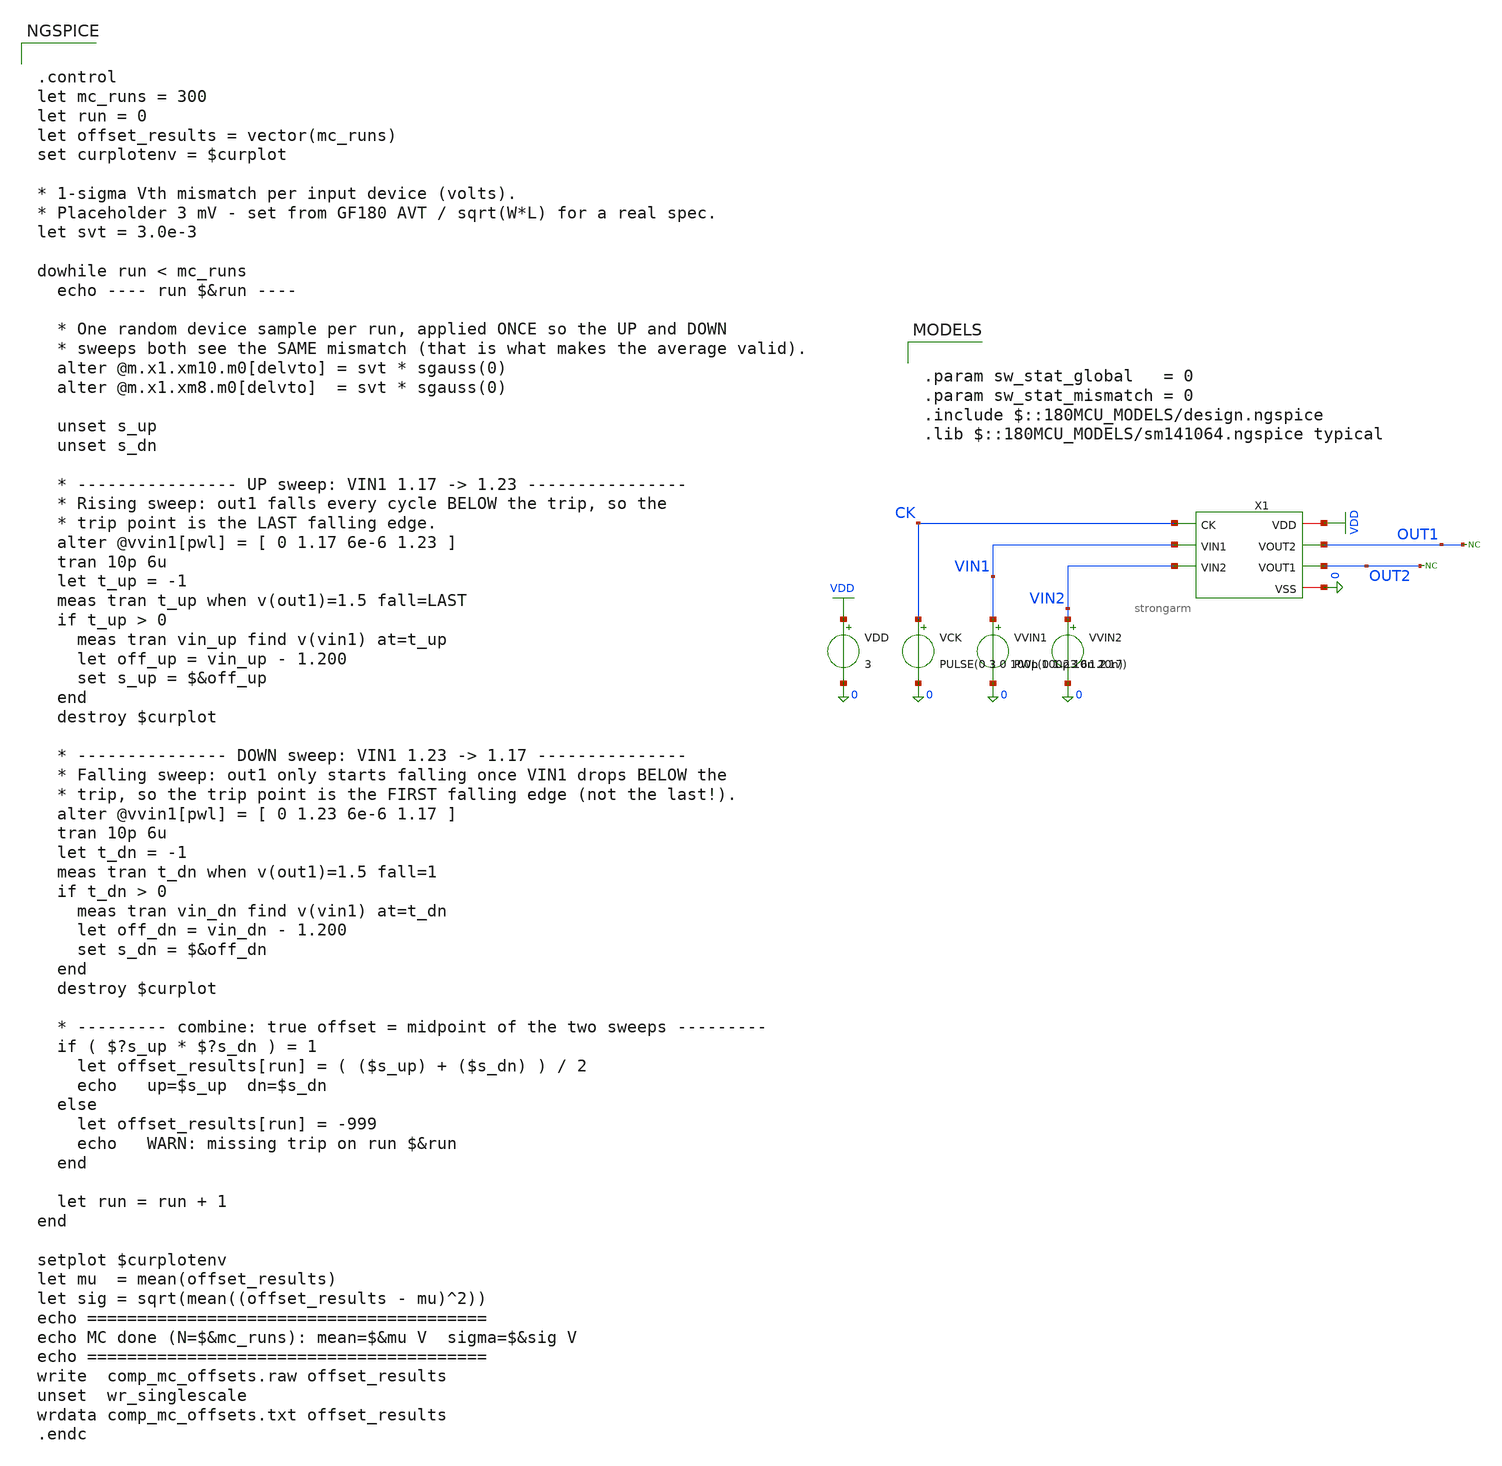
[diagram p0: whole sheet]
** sch_path: comparator/schematic/strongarm_mc_tb.sch
**.subckt strongarm_mc_tb
X1 VDD CK OUT1 OUT2 VIN1 VIN2 0 strongarm
VVIN2 VIN2 0 1.2
VVIN1 VIN1 0 PWL(0 1.23 6u 1.17)
VDD VDD 0 3
VCK CK 0 PULSE(0 3 0 100p 100p 10n 20n)
* noconn OUT2
* noconn OUT1
**** begin user architecture code

.param sw_stat_global   = 0
.param sw_stat_mismatch = 0
.include $::180MCU_MODELS/design.ngspice
.lib $::180MCU_MODELS/sm141064.ngspice typical



.control
let mc_runs = 300
let run = 0
let offset_results = vector(mc_runs)
set curplotenv = $curplot

* 1-sigma Vth mismatch per input device (volts).
* Placeholder 3 mV - set from GF180 AVT / sqrt(W*L) for a real spec.
let svt = 3.0e-3

dowhile run < mc_runs
  echo ---- run $&run ----

  * One random device sample per run, applied ONCE so the UP and DOWN
  * sweeps both see the SAME mismatch (that is what makes the average valid).
  alter @m.x1.xm10.m0[delvto] = svt * sgauss(0)
  alter @m.x1.xm8.m0[delvto]  = svt * sgauss(0)

  unset s_up
  unset s_dn

  * ---------------- UP sweep: VIN1 1.17 -> 1.23 ----------------
  * Rising sweep: out1 falls every cycle BELOW the trip, so the
  * trip point is the LAST falling edge.
  alter @vvin1[pwl] = [ 0 1.17 6e-6 1.23 ]
  tran 10p 6u
  let t_up = -1
  meas tran t_up when v(out1)=1.5 fall=LAST
  if t_up > 0
    meas tran vin_up find v(vin1) at=t_up
    let off_up = vin_up - 1.200
    set s_up = $&off_up
  end
  destroy $curplot

  * --------------- DOWN sweep: VIN1 1.23 -> 1.17 ---------------
  * Falling sweep: out1 only starts falling once VIN1 drops BELOW the
  * trip, so the trip point is the FIRST falling edge (not the last!).
  alter @vvin1[pwl] = [ 0 1.23 6e-6 1.17 ]
  tran 10p 6u
  let t_dn = -1
  meas tran t_dn when v(out1)=1.5 fall=1
  if t_dn > 0
    meas tran vin_dn find v(vin1) at=t_dn
    let off_dn = vin_dn - 1.200
    set s_dn = $&off_dn
  end
  destroy $curplot

  * --------- combine: true offset = midpoint of the two sweeps ---------
  if ( $?s_up * $?s_dn ) = 1
    let offset_results[run] = ( ($s_up) + ($s_dn) ) / 2
    echo   up=$s_up  dn=$s_dn
  else
    let offset_results[run] = -999
    echo   WARN: missing trip on run $&run
  end

  let run = run + 1
end

setplot $curplotenv
let mu  = mean(offset_results)
let sig = sqrt(mean((offset_results - mu)^2))
echo ========================================
echo MC done (N=$&mc_runs): mean=$&mu V  sigma=$&sig V
echo ========================================
write  comp_mc_offsets.raw offset_results
unset  wr_singlescale
wrdata comp_mc_offsets.txt offset_results
.endc


**** end user architecture code
**.ends

* expanding   symbol:  comparator/schematic/strongarm.sym # of pins=7
** sym_path: comparator/schematic/strongarm.sym
** sch_path: comparator/schematic/strongarm.sch
.subckt strongarm VDD CK VOUT2 VOUT1 VIN1 VIN2 VSS
*.opin VOUT1
*.opin VOUT2
*.ipin VIN1
*.ipin VIN2
*.ipin CK
*.iopin VDD
*.iopin VSS
XM1 VOUT2 VOUT1 net1 net1 nfet_03v3 L=0.28u W=0.22u nf=1 ad='int((nf+1)/2) * W/nf * 0.18u' as='int((nf+2)/2) * W/nf * 0.18u'
+ pd='2*int((nf+1)/2) * (W/nf + 0.18u)' ps='2*int((nf+2)/2) * (W/nf + 0.18u)' nrd='0.18u / W' nrs='0.18u / W'
+ sa=0 sb=0 sd=0 m=1
XM2 VOUT1 VOUT2 VDD VDD pfet_03v3 L=0.28u W=0.22u nf=1 ad='int((nf+1)/2) * W/nf * 0.18u' as='int((nf+2)/2) * W/nf * 0.18u'
+ pd='2*int((nf+1)/2) * (W/nf + 0.18u)' ps='2*int((nf+2)/2) * (W/nf + 0.18u)' nrd='0.18u / W' nrs='0.18u / W'
+ sa=0 sb=0 sd=0 m=1
XM3 VOUT1 CK VDD VDD pfet_03v3 L=0.28u W=0.22u nf=1 ad='int((nf+1)/2) * W/nf * 0.18u' as='int((nf+2)/2) * W/nf * 0.18u'
+ pd='2*int((nf+1)/2) * (W/nf + 0.18u)' ps='2*int((nf+2)/2) * (W/nf + 0.18u)' nrd='0.18u / W' nrs='0.18u / W'
+ sa=0 sb=0 sd=0 m=1
XM4 net3 CK VDD VDD pfet_03v3 L=0.28u W=0.22u nf=1 ad='int((nf+1)/2) * W/nf * 0.18u' as='int((nf+2)/2) * W/nf * 0.18u'
+ pd='2*int((nf+1)/2) * (W/nf + 0.18u)' ps='2*int((nf+2)/2) * (W/nf + 0.18u)' nrd='0.18u / W' nrs='0.18u / W'
+ sa=0 sb=0 sd=0 m=1
XM5 net1 CK VDD VDD pfet_03v3 L=0.28u W=0.22u nf=1 ad='int((nf+1)/2) * W/nf * 0.18u' as='int((nf+2)/2) * W/nf * 0.18u'
+ pd='2*int((nf+1)/2) * (W/nf + 0.18u)' ps='2*int((nf+2)/2) * (W/nf + 0.18u)' nrd='0.18u / W' nrs='0.18u / W'
+ sa=0 sb=0 sd=0 m=1
XM6 VOUT2 CK VDD VDD pfet_03v3 L=0.28u W=0.22u nf=1 ad='int((nf+1)/2) * W/nf * 0.18u' as='int((nf+2)/2) * W/nf * 0.18u'
+ pd='2*int((nf+1)/2) * (W/nf + 0.18u)' ps='2*int((nf+2)/2) * (W/nf + 0.18u)' nrd='0.18u / W' nrs='0.18u / W'
+ sa=0 sb=0 sd=0 m=1
XM7 VOUT2 VOUT1 VDD VDD pfet_03v3 L=0.28u W=0.22u nf=1 ad='int((nf+1)/2) * W/nf * 0.18u' as='int((nf+2)/2) * W/nf * 0.18u'
+ pd='2*int((nf+1)/2) * (W/nf + 0.18u)' ps='2*int((nf+2)/2) * (W/nf + 0.18u)' nrd='0.18u / W' nrs='0.18u / W'
+ sa=0 sb=0 sd=0 m=1
XM8 net1 VIN2 net2 net2 nfet_03v3 L=0.28u W=0.22u nf=1 ad='int((nf+1)/2) * W/nf * 0.18u' as='int((nf+2)/2) * W/nf * 0.18u'
+ pd='2*int((nf+1)/2) * (W/nf + 0.18u)' ps='2*int((nf+2)/2) * (W/nf + 0.18u)' nrd='0.18u / W' nrs='0.18u / W'
+ sa=0 sb=0 sd=0 m=1
XM9 VOUT1 VOUT2 net3 net3 nfet_03v3 L=0.28u W=0.22u nf=1 ad='int((nf+1)/2) * W/nf * 0.18u' as='int((nf+2)/2) * W/nf * 0.18u'
+ pd='2*int((nf+1)/2) * (W/nf + 0.18u)' ps='2*int((nf+2)/2) * (W/nf + 0.18u)' nrd='0.18u / W' nrs='0.18u / W'
+ sa=0 sb=0 sd=0 m=1
XM10 net3 VIN1 net2 net2 nfet_03v3 L=0.28u W=0.22u nf=1 ad='int((nf+1)/2) * W/nf * 0.18u' as='int((nf+2)/2) * W/nf * 0.18u'
+ pd='2*int((nf+1)/2) * (W/nf + 0.18u)' ps='2*int((nf+2)/2) * (W/nf + 0.18u)' nrd='0.18u / W' nrs='0.18u / W'
+ sa=0 sb=0 sd=0 m=1
XM11 net2 CK VSS net2 nfet_03v3 L=0.28u W=0.22u nf=1 ad='int((nf+1)/2) * W/nf * 0.18u' as='int((nf+2)/2) * W/nf * 0.18u'
+ pd='2*int((nf+1)/2) * (W/nf + 0.18u)' ps='2*int((nf+2)/2) * (W/nf + 0.18u)' nrd='0.18u / W' nrs='0.18u / W'
+ sa=0 sb=0 sd=0 m=1
.ends

.GLOBAL VDD
.end
